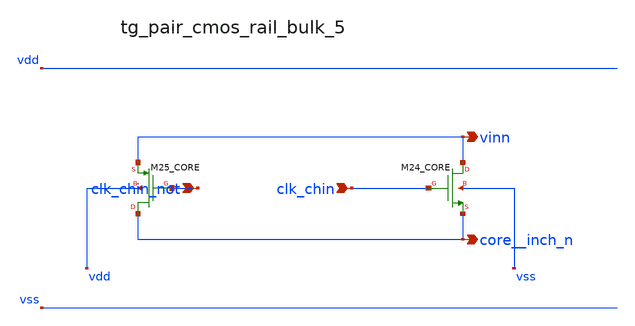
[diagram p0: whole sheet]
** sch_path: analog-db/raw/ia_006_fan_chopper_cmfb/hier/blocks/tg_pair_cmos_rail_bulk_5.sch
**.subckt tg_pair_cmos_rail_bulk_5 clk_chin_not clk_chin vinn core__inch_n
*.ipin clk_chin_not
*.ipin clk_chin
*.opin vinn
*.opin core__inch_n
XM24_CORE vinn clk_chin core__inch_n vss sg13_lv_nmos w=x_dut_xm24_core_w l=x_dut_xm24_core_l ng=1
+ m=x_dut_xm24_core_m
XM25_CORE core__inch_n clk_chin_not vinn vdd sg13_lv_pmos w=x_dut_xm25_core_w l=x_dut_xm25_core_l
+ ng=1 m=x_dut_xm25_core_m
**.ends
.end
